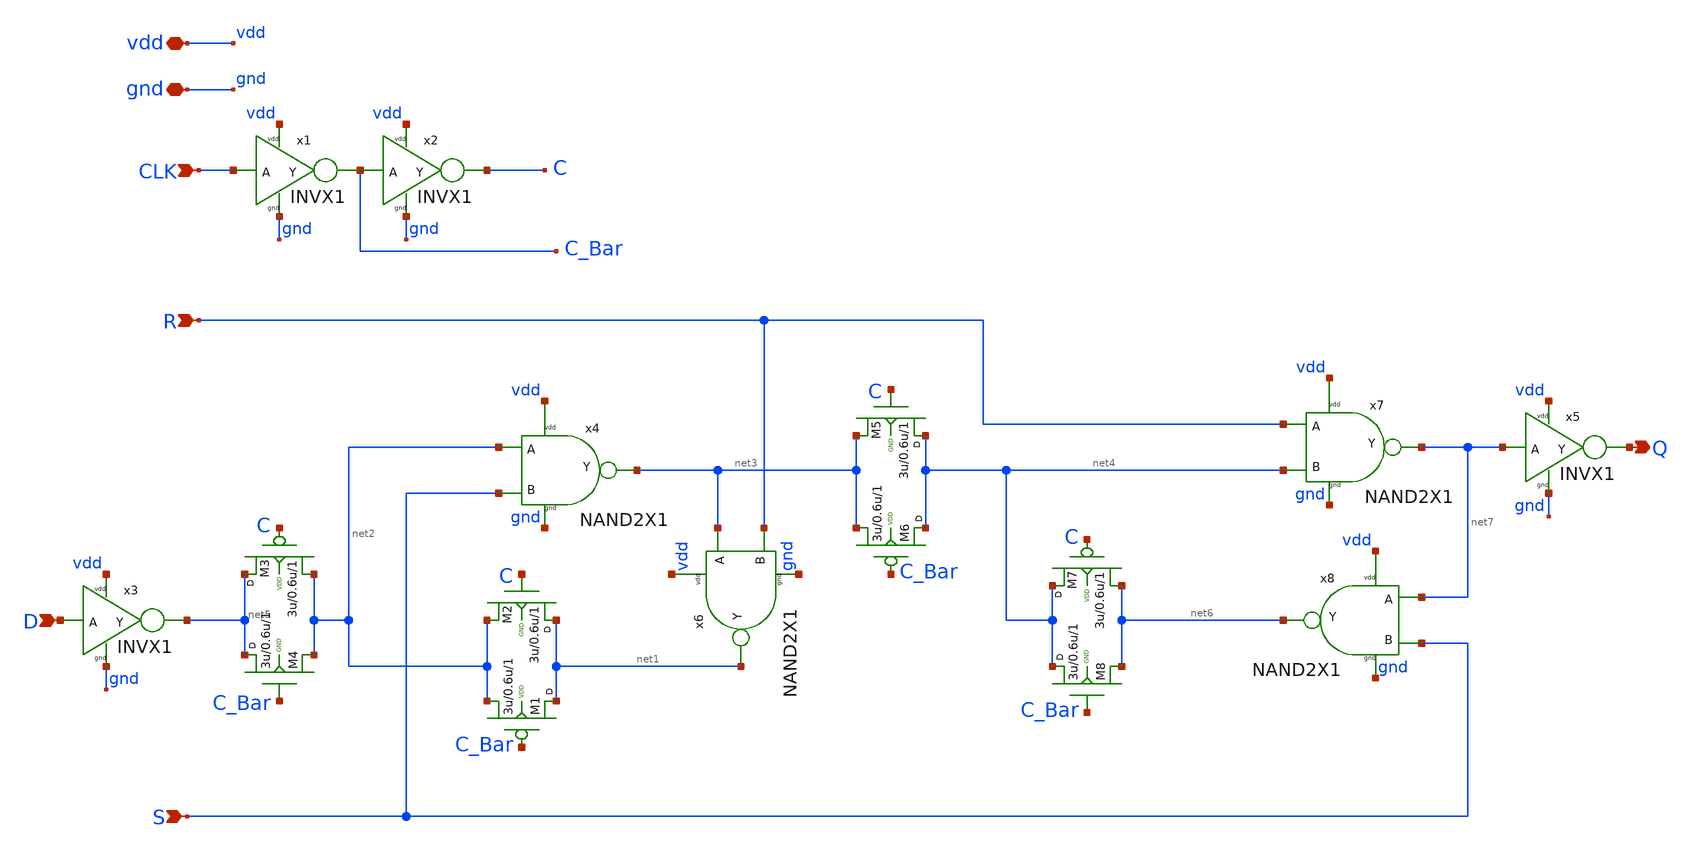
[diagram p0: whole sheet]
** sch_path: Tutorials/1-4_StdCell_DFFSR/Layout/2_NAND2_SR_AB/DFFSR.sch
**.subckt DFFSR CLK D Q S R vdd gnd
*.ipin CLK
*.ipin D
*.opin Q
*.ipin S
*.ipin R
*.iopin vdd
*.iopin gnd
M1 net1 C_Bar net2 VDD pfet w=3u l=0.6u m=1
M2 net1 C net2 GND nfet w=3u l=0.6u m=1
M3 net5 C net2 VDD pfet w=3u l=0.6u m=1
M4 net5 C_Bar net2 GND nfet w=3u l=0.6u m=1
M6 net4 C_Bar net3 VDD pfet w=3u l=0.6u m=1
M5 net4 C net3 GND nfet w=3u l=0.6u m=1
M7 net4 C net6 VDD pfet w=3u l=0.6u m=1
M8 net4 C_Bar net6 GND nfet w=3u l=0.6u m=1
x1 CLK C_Bar vdd gnd INVX1
x2 C_Bar C vdd gnd INVX1
x4 net2 S net3 vdd gnd NAND2X1
x6 net3 R net1 vdd gnd NAND2X1
x7 R net4 net7 vdd gnd NAND2X1
x8 net7 S net6 vdd gnd NAND2X1
x3 D net5 vdd gnd INVX1
x5 net7 Q vdd gnd INVX1
**.ends

* expanding   symbol:  /home/goodkook/ETRI050_DesignKit/Tutorials/1-4_StdCell_DFFSR/Sch/INVX1.sym #
*+ of pins=4
** sym_path: Tutorials/1-4_StdCell_DFFSR/Sch/INVX1.sym
** sch_path: Tutorials/1-4_StdCell_DFFSR/Sch/INVX1.sch
.subckt INVX1 A Y vdd gnd
*.ipin A
*.opin Y
*.iopin vdd
*.iopin gnd
M1 Y A gnd GND nfet w=3u l=0.6u m=1
M2 Y A vdd VDD pfet w=6u l=0.6u m=1
.ends


* expanding   symbol:  /home/goodkook/ETRI050_DesignKit/Tutorials/1-4_StdCell_DFFSR/Sch/NAND2X1.sym
*+ # of pins=5
** sym_path: Tutorials/1-4_StdCell_DFFSR/Sch/NAND2X1.sym
** sch_path: Tutorials/1-4_StdCell_DFFSR/Sch/NAND2X1.sch
.subckt NAND2X1 A B Y vdd gnd
*.ipin A
*.ipin B
*.opin Y
*.iopin vdd
*.iopin gnd
M1 Y B net1 GND nfet w=6u l=0.6u m=1
M2 Y B vdd VDD pfet w=6u l=0.6u m=1
M3 net1 A gnd GND nfet w=6u l=0.6u m=1
M4 Y A vdd VDD pfet w=6u l=0.6u m=1
.ends

.end
